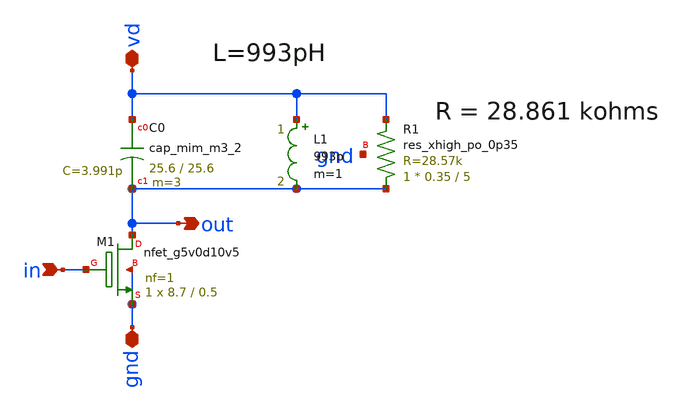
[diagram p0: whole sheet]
** sch_path: xschem-2.45GHz/ask-2.45G-0.sch
**.subckt ask-2.45G-0 gnd in out vd
*.iopin gnd
*.ipin in
*.opin out
*.iopin vd
XC0 vd out sky130_fd_pr__cap_mim_m3_2 W=25.6 L=25.6 MF=3 m=3
XM1 out in gnd gnd sky130_fd_pr__nfet_g5v0d10v5 L=0.5 W=8.7 nf=1 ad='int((nf+1)/2) * W/nf * 0.29' as='int((nf+2)/2) * W/nf * 0.29'
+ pd='2*int((nf+1)/2) * (W/nf + 0.29)' ps='2*int((nf+2)/2) * (W/nf + 0.29)' nrd='0.29 / W' nrs='0.29 / W'
+ sa=0 sb=0 sd=0 mult=1 m=1
XR1 out vd gnd sky130_fd_pr__res_xhigh_po_0p35 L=5 mult=1 m=1
L1 vd out 993p m=1
**.ends
.end
